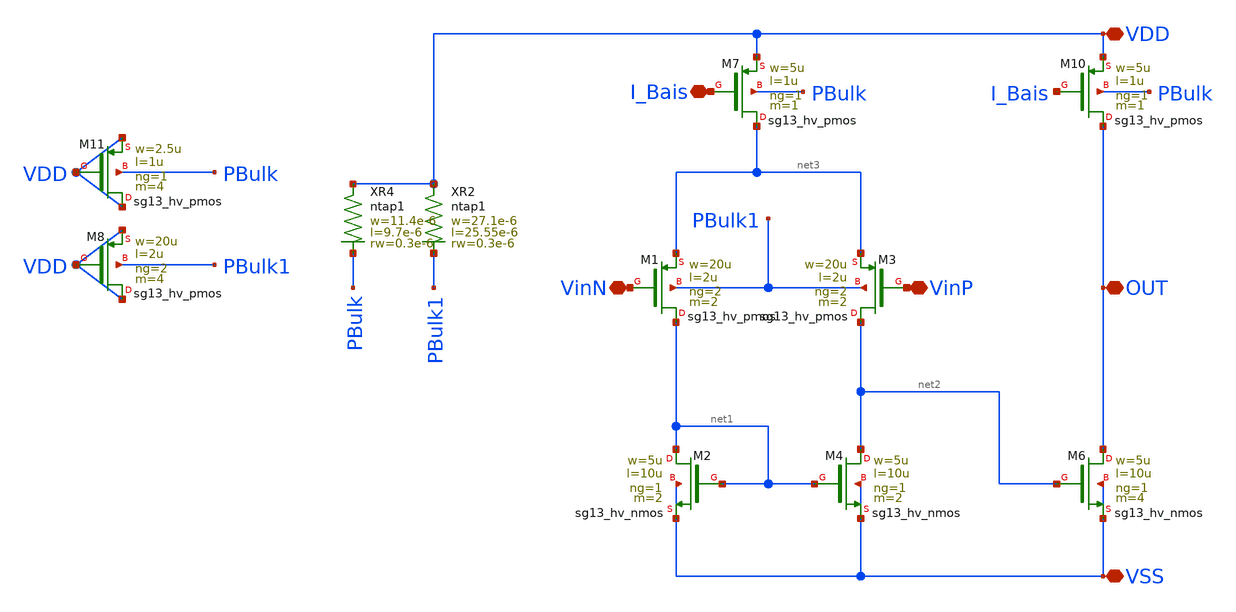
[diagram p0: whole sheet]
** sch_path: LVS/LVS_Sch/Comp_2Stage.sch
**.subckt Comp_2Stage OUT VSS VDD VinP VinN I_Bais
*.iopin OUT
*.iopin VSS
*.iopin VDD
*.iopin VinP
*.iopin VinN
*.iopin I_Bais
XM2 net1 net1 VSS VSS sg13_hv_nmos w=5u l=10u ng=1 m=2 mm_ok=1
XM4 net2 net1 VSS VSS sg13_hv_nmos w=5u l=10u ng=1 m=2 mm_ok=1
XM1 net1 VinN net3 PBulk1 sg13_hv_pmos w=20u l=2u ng=2 m=2 mm_ok=1
XM3 net2 VinP net3 PBulk1 sg13_hv_pmos w=20u l=2u ng=2 m=2 mm_ok=1
XM8 VDD VDD VDD PBulk1 sg13_hv_pmos w=20u l=2u ng=2 m=4 mm_ok=1
XR2 VDD PBulk1 ntap1 R=2.189 w=27.1e-6 l=25.55e-6 rw=0.3e-6
XM6 OUT net2 VSS VSS sg13_hv_nmos w=5u l=10u ng=1 m=4 mm_ok=1
XM7 net3 I_Bais VDD PBulk sg13_hv_pmos w=5u l=1u ng=1 m=1 mm_ok=1
XM10 OUT I_Bais VDD PBulk sg13_hv_pmos w=5u l=1u ng=1 m=1 mm_ok=1
XM11 VDD VDD VDD PBulk sg13_hv_pmos w=2.5u l=1u ng=1 m=4 mm_ok=1
XR4 VDD PBulk ntap1 R=5.559 w=11.4e-6 l=9.7e-6 rw=0.3e-6
**.ends
.end
